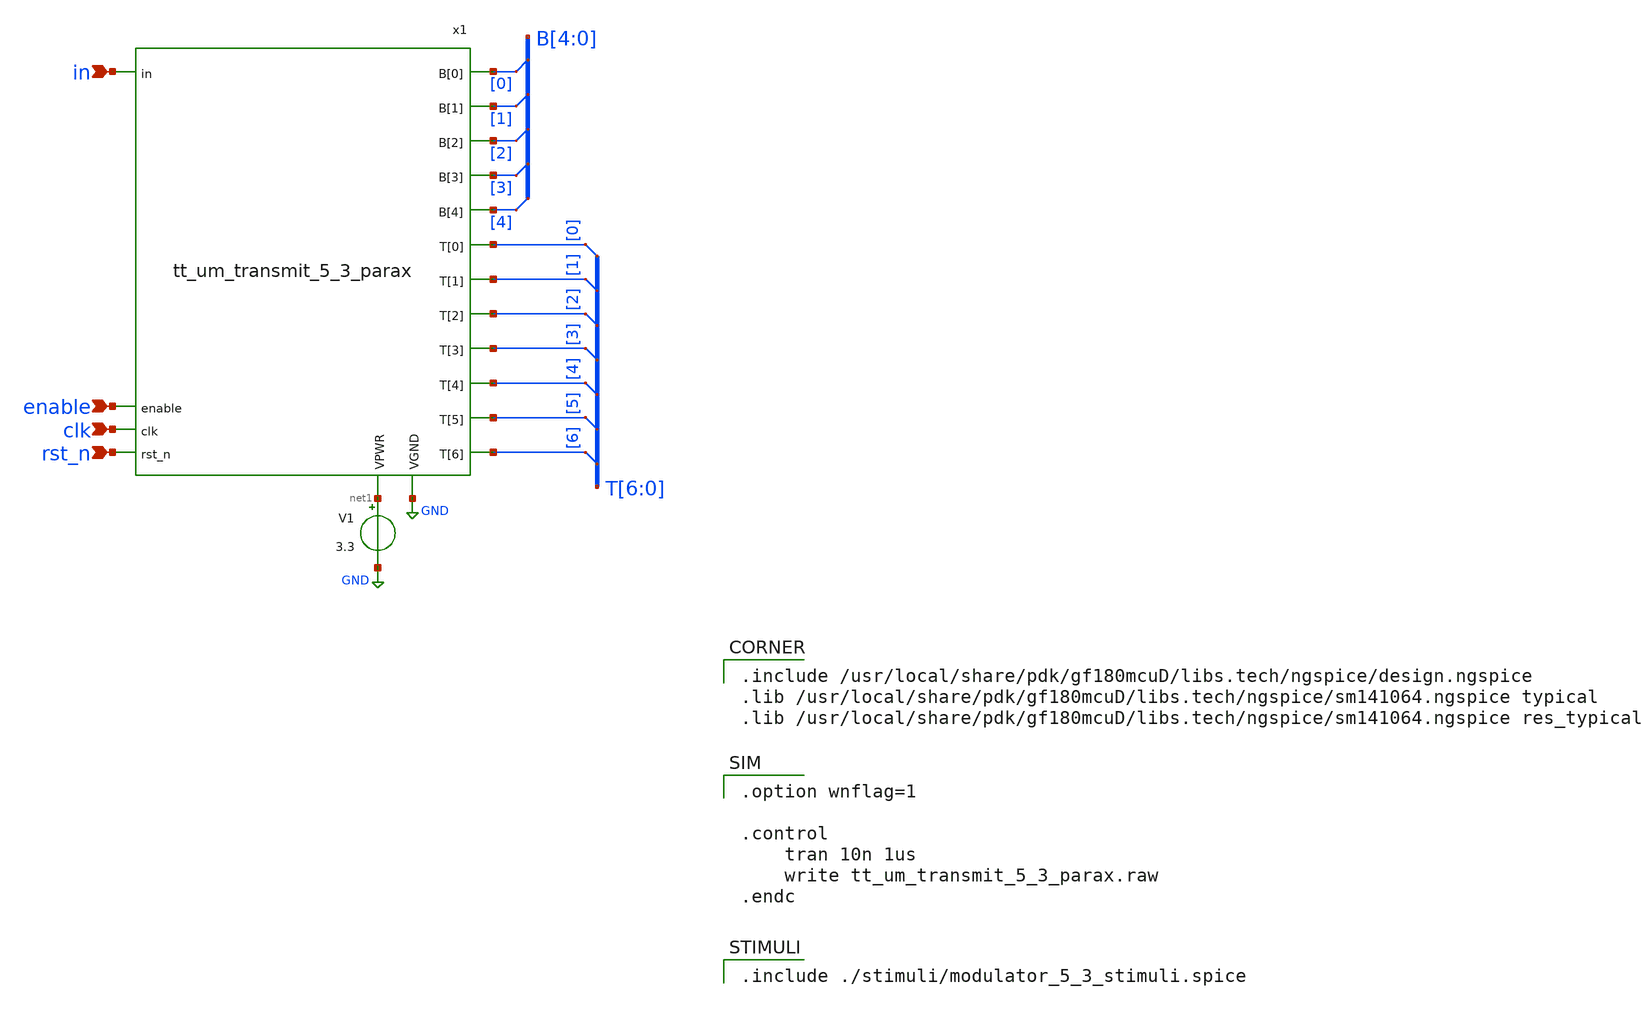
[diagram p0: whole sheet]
** sch_path: xschem/tb_transmit_parax.sch
**.subckt tb_transmit_parax in enable clk rst_n
*.ipin in
*.ipin enable
*.ipin clk
*.ipin rst_n
x1 B[0] B[1] B[2] B[3] B[4] T[0] T[1] T[2] T[3] T[4] T[5] T[6] GND net1 clk enable in rst_n
+ tt_um_transmit_5_3_parax
V1 net1 GND 3.3
* tap: B[4:0] --> B[0]
* tap: B[4:0] --> B[1]
* tap: B[4:0] --> B[2]
* tap: B[4:0] --> B[3]
* tap: B[4:0] --> B[4]
* tap: T[6:0] --> T[0]
* tap: T[6:0] --> T[1]
* tap: T[6:0] --> T[2]
* tap: T[6:0] --> T[3]
* tap: T[6:0] --> T[4]
* tap: T[6:0] --> T[5]
* tap: T[6:0] --> T[6]
**** begin user architecture code

.option wnflag=1

.control
    tran 10n 1us
    write tt_um_transmit_5_3_parax.raw
.endc



.include ./stimuli/modulator_5_3_stimuli.spice


.include /usr/local/share/pdk/gf180mcuD/libs.tech/ngspice/design.ngspice
.lib /usr/local/share/pdk/gf180mcuD/libs.tech/ngspice/sm141064.ngspice typical
.lib /usr/local/share/pdk/gf180mcuD/libs.tech/ngspice/sm141064.ngspice res_typical

**** end user architecture code
**.ends

* expanding   symbol:  tt_um_transmit_5_3_parax.sym # of pins=18
** sym_path: xschem/tt_um_transmit_5_3_parax.sym
.include ../../mag/spice/tt_um_transmit_5_3_parax.spice
.GLOBAL GND
.end
